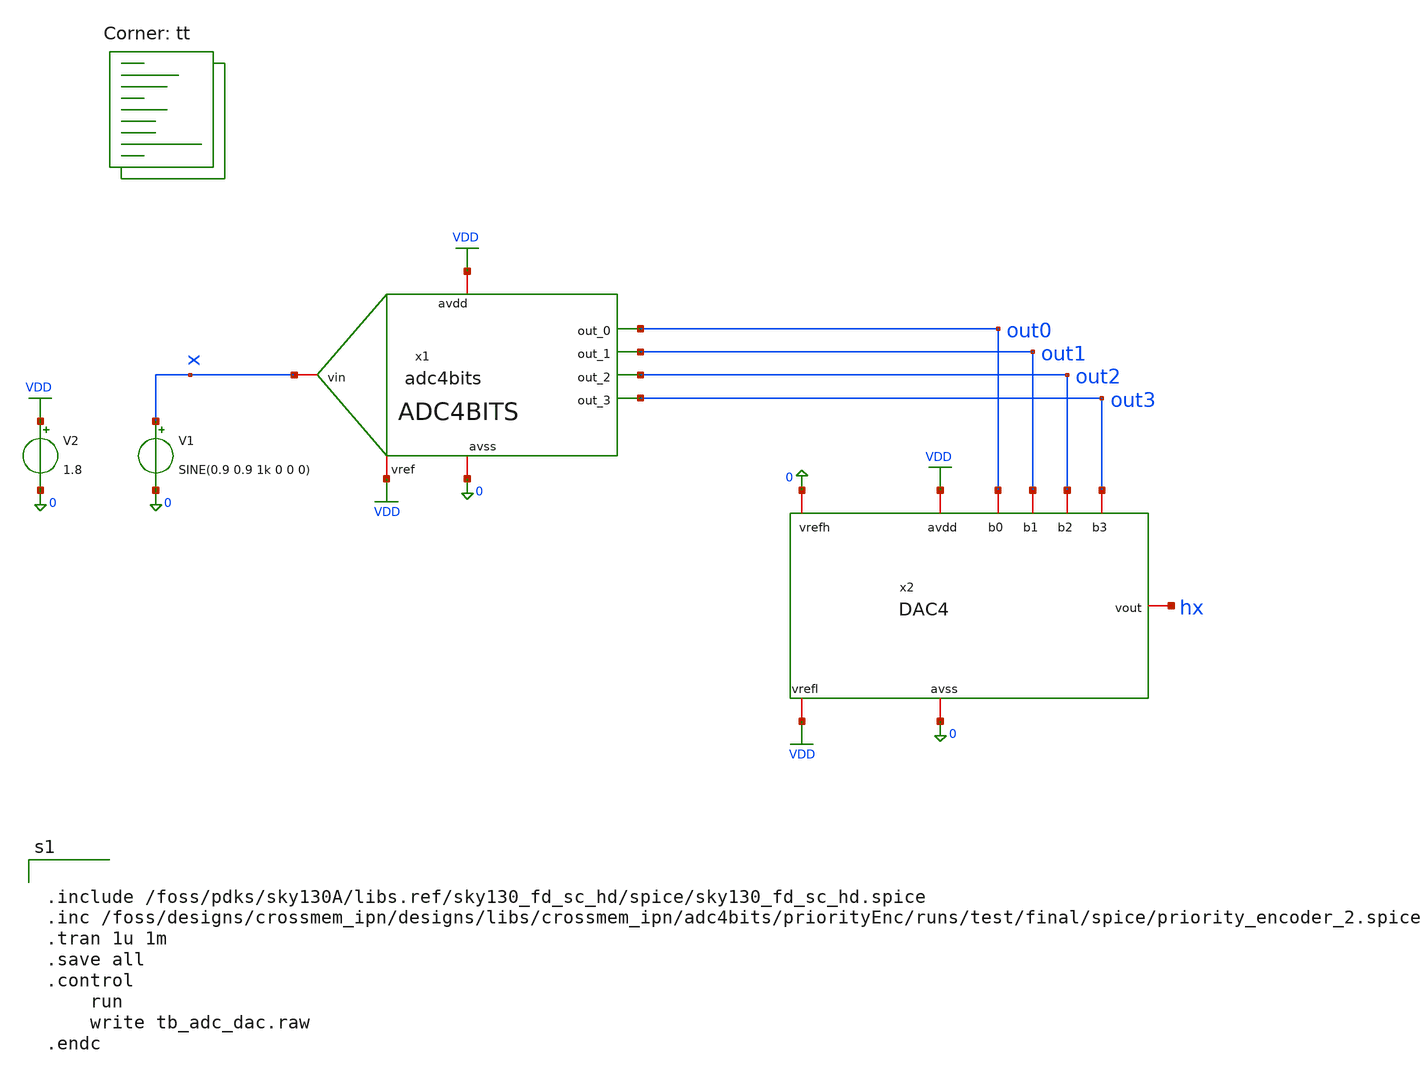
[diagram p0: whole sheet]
** sch_path: designs/libs/crossmem_ipn/tb_adc_dac.sch
**.subckt tb_adc_dac
V1 x 0 SINE(0.9 0.9 1k 0 0 0)
x1 x VDD out0 out1 out2 out3 0 VDD adc4bits
V2 VDD 0 1.8
x2 VDD out0 out1 0 out2 0 hx VDD out3 DAC4
**** begin user architecture code


.include /foss/pdks/sky130A/libs.ref/sky130_fd_sc_hd/spice/sky130_fd_sc_hd.spice
.inc /foss/designs/crossmem_ipn/designs/libs/crossmem_ipn/adc4bits/priorityEnc/runs/test/final/spice/priority_encoder_2.spice
.tran 1u 1m
.save all
.control
	run
	write tb_adc_dac.raw
.endc


.lib $::SKYWATER_MODELS/sky130.lib.spice tt
**** end user architecture code
**.ends
.GLOBAL VDD
.end
